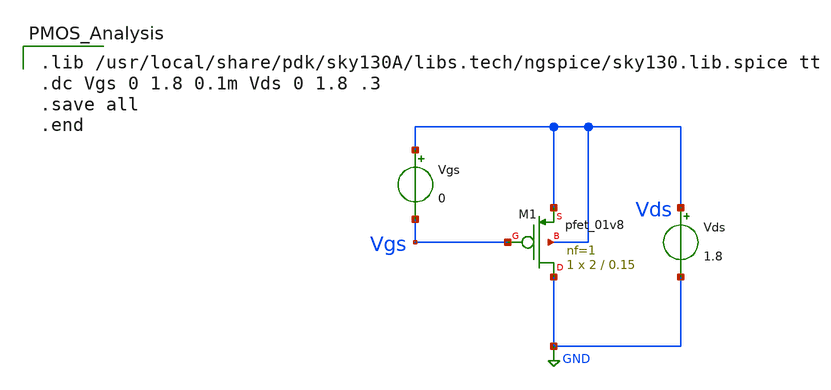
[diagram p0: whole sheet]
** sch_path: Projects/Characteristics_of_MOS_Devices_Utilizing_SKY130_Process_Design_Kit_with_Xschem_and_Ngspice/assets/files/pmos_analysis.sch
**.subckt pmos_analysis
XM1 GND Vgs Vds Vds sky130_fd_pr__pfet_01v8 L=0.15 W=2 nf=1 ad='int((nf+1)/2) * W/nf * 0.29' as='int((nf+2)/2) * W/nf * 0.29'
+ pd='2*int((nf+1)/2) * (W/nf + 0.29)' ps='2*int((nf+2)/2) * (W/nf + 0.29)' nrd='0.29 / W' nrs='0.29 / W'
+ sa=0 sb=0 sd=0 mult=1 m=1
Vgs Vds Vgs 0
Vds Vds GND 1.8
**** begin user architecture code

.lib /usr/local/share/pdk/sky130A/libs.tech/ngspice/sky130.lib.spice tt
.dc Vgs 0 1.8 0.1m Vds 0 1.8 .3
.save all
.end

**** end user architecture code
**.ends
.GLOBAL GND
.end
